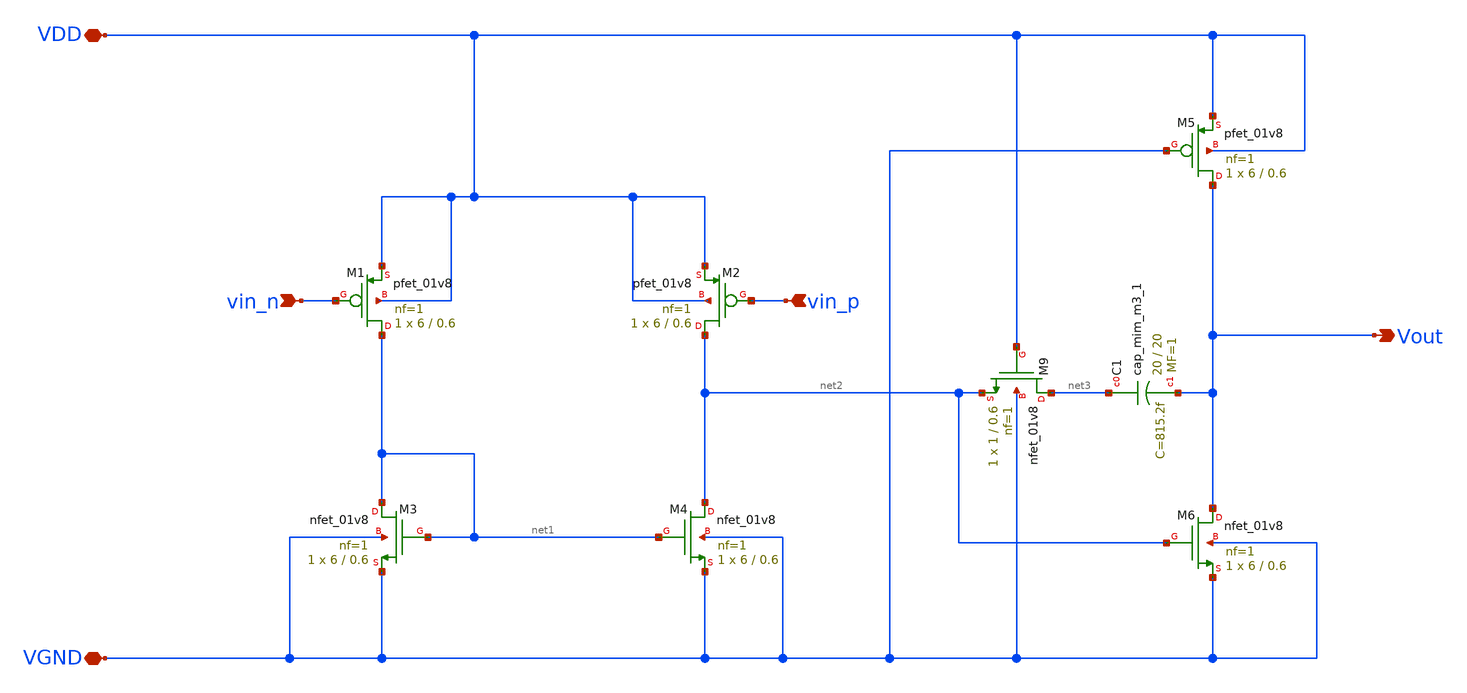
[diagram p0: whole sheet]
** sch_path: xschem/ds_opamp.sch
**.subckt ds_opamp vin_n vin_p Vout VDD VGND
*.ipin vin_n
*.ipin vin_p
*.opin Vout
*.iopin VDD
*.iopin VGND
XM1 net1 vin_n VDD VDD sky130_fd_pr__pfet_01v8 L=0.6 W=6 nf=1 ad='W * 0.29' as='W * 0.29' pd='2 * (W + 0.29)'
+ ps='2 * (W + 0.29)' nrd='0.29 / W' nrs='0.29 / W' sa=0 sb=0 sd=0 mult=1 m=1
XM2 net2 vin_p VDD VDD sky130_fd_pr__pfet_01v8 L=0.6 W=6 nf=1 ad='W * 0.29' as='W * 0.29' pd='2 * (W + 0.29)'
+ ps='2 * (W + 0.29)' nrd='0.29 / W' nrs='0.29 / W' sa=0 sb=0 sd=0 mult=1 m=1
XM3 net1 net1 VGND VGND sky130_fd_pr__nfet_01v8 L=0.6 W=6 nf=1 ad='W * 0.29' as='W * 0.29' pd='2 * (W + 0.29)'
+ ps='2 * (W + 0.29)' nrd='0.29 / W' nrs='0.29 / W' sa=0 sb=0 sd=0 mult=1 m=1
XM4 net2 net1 VGND VGND sky130_fd_pr__nfet_01v8 L=0.6 W=6 nf=1 ad='W * 0.29' as='W * 0.29' pd='2 * (W + 0.29)'
+ ps='2 * (W + 0.29)' nrd='0.29 / W' nrs='0.29 / W' sa=0 sb=0 sd=0 mult=1 m=1
XM9 net3 VDD net2 VGND sky130_fd_pr__nfet_01v8 L=0.6 W=1 nf=1 ad='W * 0.29' as='W * 0.29' pd='2 * (W + 0.29)'
+ ps='2 * (W + 0.29)' nrd='0.29 / W' nrs='0.29 / W' sa=0 sb=0 sd=0 mult=1 m=1
XC1 net3 Vout sky130_fd_pr__cap_mim_m3_1 W=20 L=20 MF=1 m=1
XM6 Vout net2 VGND VGND sky130_fd_pr__nfet_01v8 L=0.6 W=6 nf=1 ad='W * 0.29' as='W * 0.29' pd='2 * (W + 0.29)'
+ ps='2 * (W + 0.29)' nrd='0.29 / W' nrs='0.29 / W' sa=0 sb=0 sd=0 mult=1 m=1
XM5 Vout VGND VDD VDD sky130_fd_pr__pfet_01v8 L=0.6 W=6 nf=1 ad='W * 0.29' as='W * 0.29' pd='2 * (W + 0.29)'
+ ps='2 * (W + 0.29)' nrd='0.29 / W' nrs='0.29 / W' sa=0 sb=0 sd=0 mult=1 m=1
**.ends
.end
